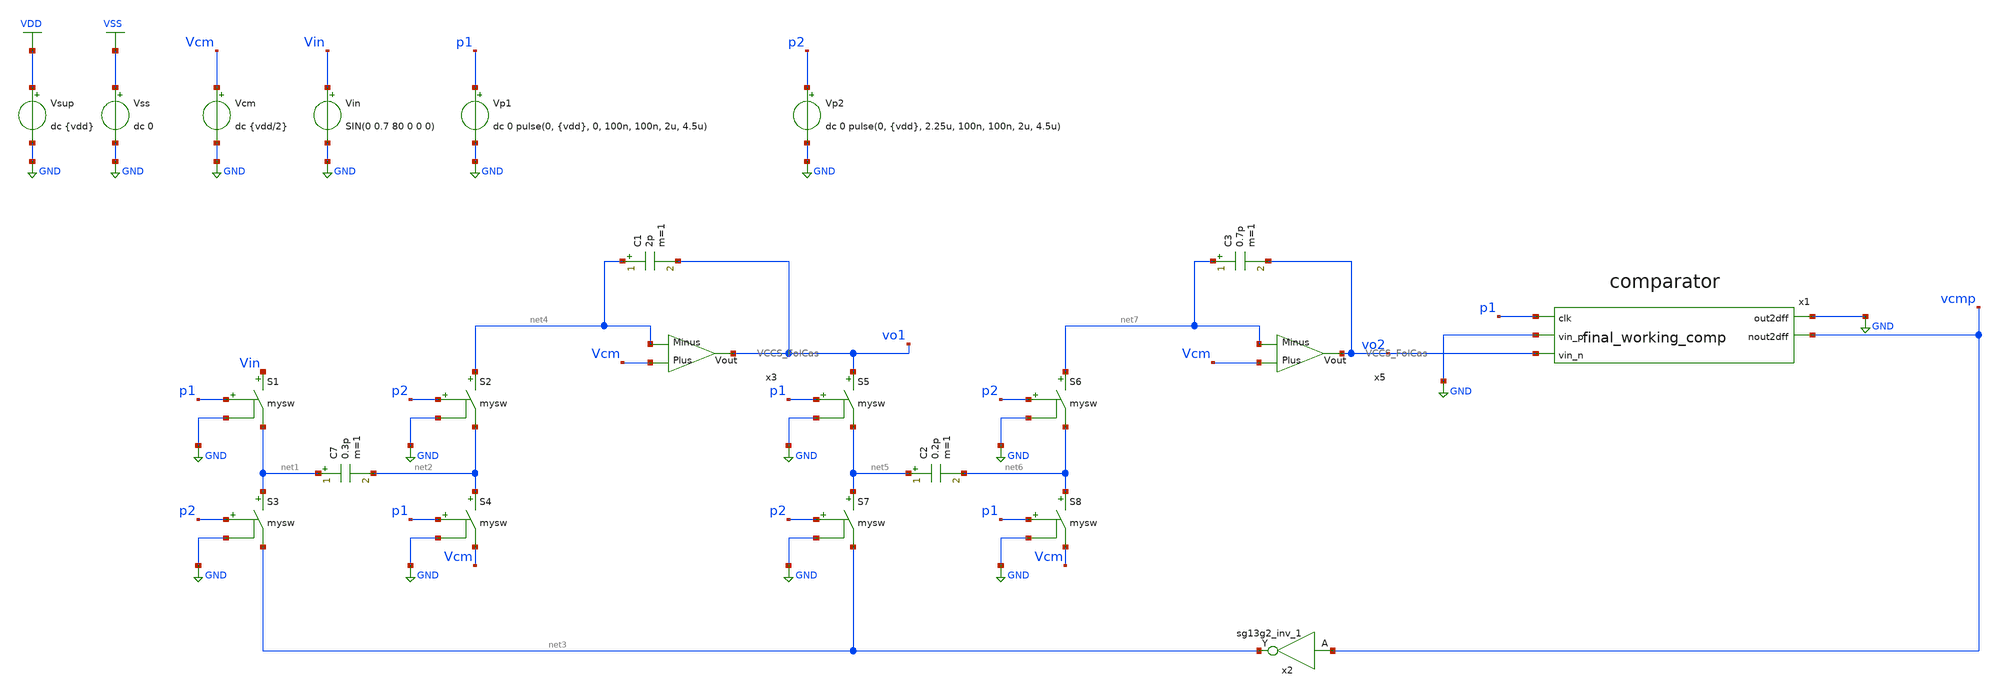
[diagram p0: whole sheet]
** sch_path: DSM/Schematics/Designs_Hrishi/RealCircuits/Real_DSM_Design.sch
**.subckt Real_DSM_Design
Vcm Vcm GND dc {vdd/2}
Vin Vin GND SIN(0 0.7 80 0 0 0)
S1 Vin net1 p1 GND mysw
S2 net4 net2 p2 GND mysw
S3 net1 net3 p2 GND mysw
S4 net2 Vcm p1 GND mysw
C7 net1 net2 0.3p m=1
C1 net4 vo1 2p m=1
S5 vo1 net5 p1 GND mysw
S6 net7 net6 p2 GND mysw
S7 net5 net3 p2 GND mysw
S8 net6 Vcm p1 GND mysw
C2 net5 net6 0.2p m=1
C3 net7 vo2 0.7p m=1
x2 net3 vcmp Vdd Vss sg13g2_inv_1
Vsup VDD GND dc {vdd}
Vss VSS GND dc 0
Vp1 p1 GND dc 0 pulse(0, {vdd}, 0, 100n, 100n, 2u, 4.5u)
Vp2 p2 GND dc 0 pulse(0, {vdd}, 2.25u, 100n, 100n, 2u, 4.5u)
x3 Vcm vo1 net4 VCCS_FolCas
x5 Vcm vo2 net7 VCCS_FolCas
x1 p1 GND GND vo2 vcmp final_working_comp
**** begin user architecture code

.lib $::SG13G2_MODELS/cornerMOSlv.lib mos_tt
.lib $::SG13G2_MODELS/cornerRES.lib res_typ
.inc /foss/pdks/ihp-sg13g2/libs.ref/sg13g2_stdcell/spice/sg13g2_stdcell.spice



.param temp=27 vdd = 1.5
.param Wnmos=2u Wpmos=4u
.param Lnmos=.13u Lpmos=.13u Lnmos2=1u
.model mysw SW vt={vdd/2} ron=0.1
.option method=gear reltol=1e-4

.control
save all
run
tran 1u 5m
plot vcmp

set wr_singlescale
set wr_vecnames
wrdata IDEAL_SwitchCap.txt vo1 vo2 vcmp p1 p2
.endc


**** end user architecture code
**.ends
.GLOBAL GND
.GLOBAL VDD
.GLOBAL VSS
.end
